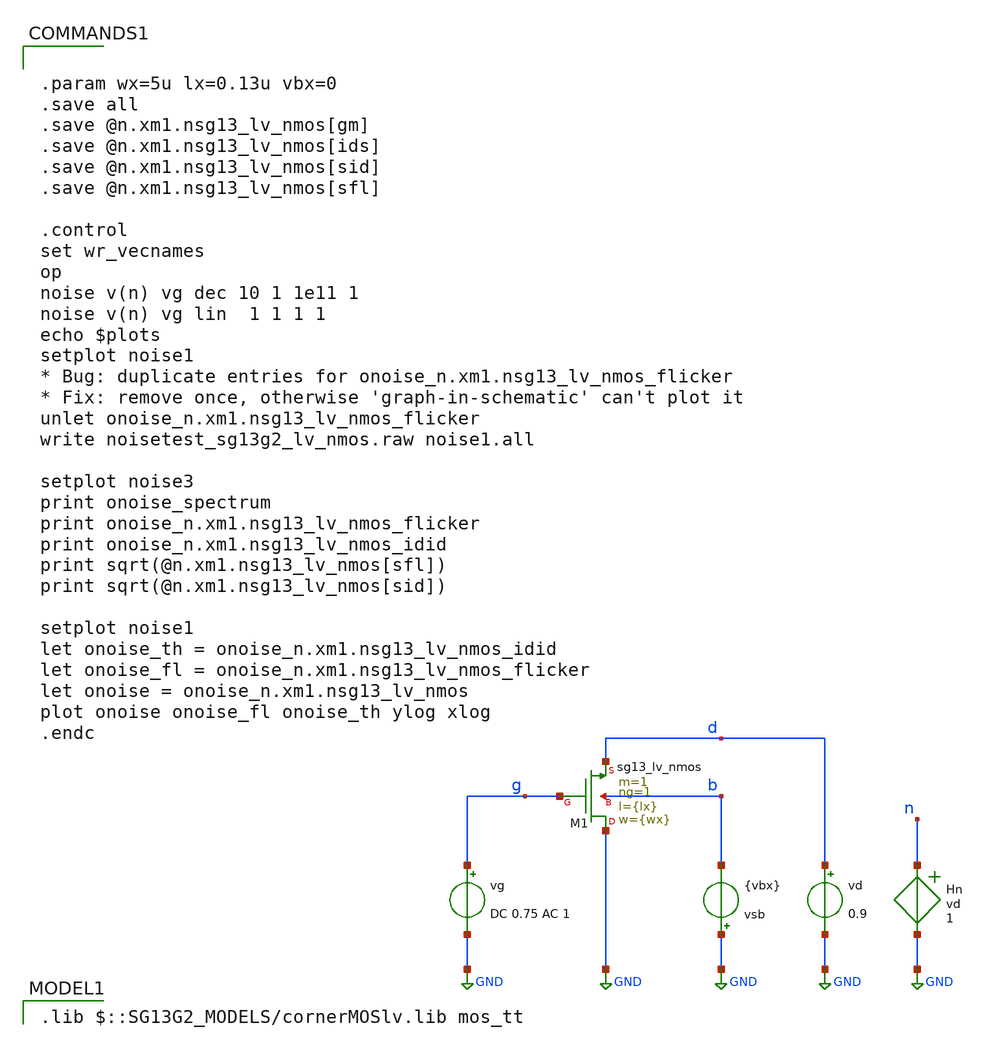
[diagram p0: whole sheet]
** sch_path: xschem/noisetest_sg13g2_lv_nmos.sch
**.subckt noisetest_sg13g2_lv_nmos
vg g GND DC 0.75 AC 1
vd d GND 0.9
vsb GND b {vbx}
Hn n GND vd 1
XM1 GND g d b sg13_lv_nmos w={wx} l={lx} ng=1 m=1 mm_ok=1
**** begin user architecture code


.param wx=5u lx=0.13u vbx=0
.save all
.save @n.xm1.nsg13_lv_nmos[gm]
.save @n.xm1.nsg13_lv_nmos[ids]
.save @n.xm1.nsg13_lv_nmos[sid]
.save @n.xm1.nsg13_lv_nmos[sfl]

.control
set wr_vecnames
op
noise v(n) vg dec 10 1 1e11 1
noise v(n) vg lin  1 1 1 1
echo $plots
setplot noise1
* Bug: duplicate entries for onoise_n.xm1.nsg13_lv_nmos_flicker
* Fix: remove once, otherwise 'graph-in-schematic' can't plot it
unlet onoise_n.xm1.nsg13_lv_nmos_flicker
write noisetest_sg13g2_lv_nmos.raw noise1.all

setplot noise3
print onoise_spectrum
print onoise_n.xm1.nsg13_lv_nmos_flicker
print onoise_n.xm1.nsg13_lv_nmos_idid
print sqrt(@n.xm1.nsg13_lv_nmos[sfl])
print sqrt(@n.xm1.nsg13_lv_nmos[sid])

setplot noise1
let onoise_th = onoise_n.xm1.nsg13_lv_nmos_idid
let onoise_fl = onoise_n.xm1.nsg13_lv_nmos_flicker
let onoise = onoise_n.xm1.nsg13_lv_nmos
plot onoise onoise_fl onoise_th ylog xlog
.endc


 .lib $::SG13G2_MODELS/cornerMOSlv.lib mos_tt

**** end user architecture code
**.ends
.GLOBAL GND
.end
